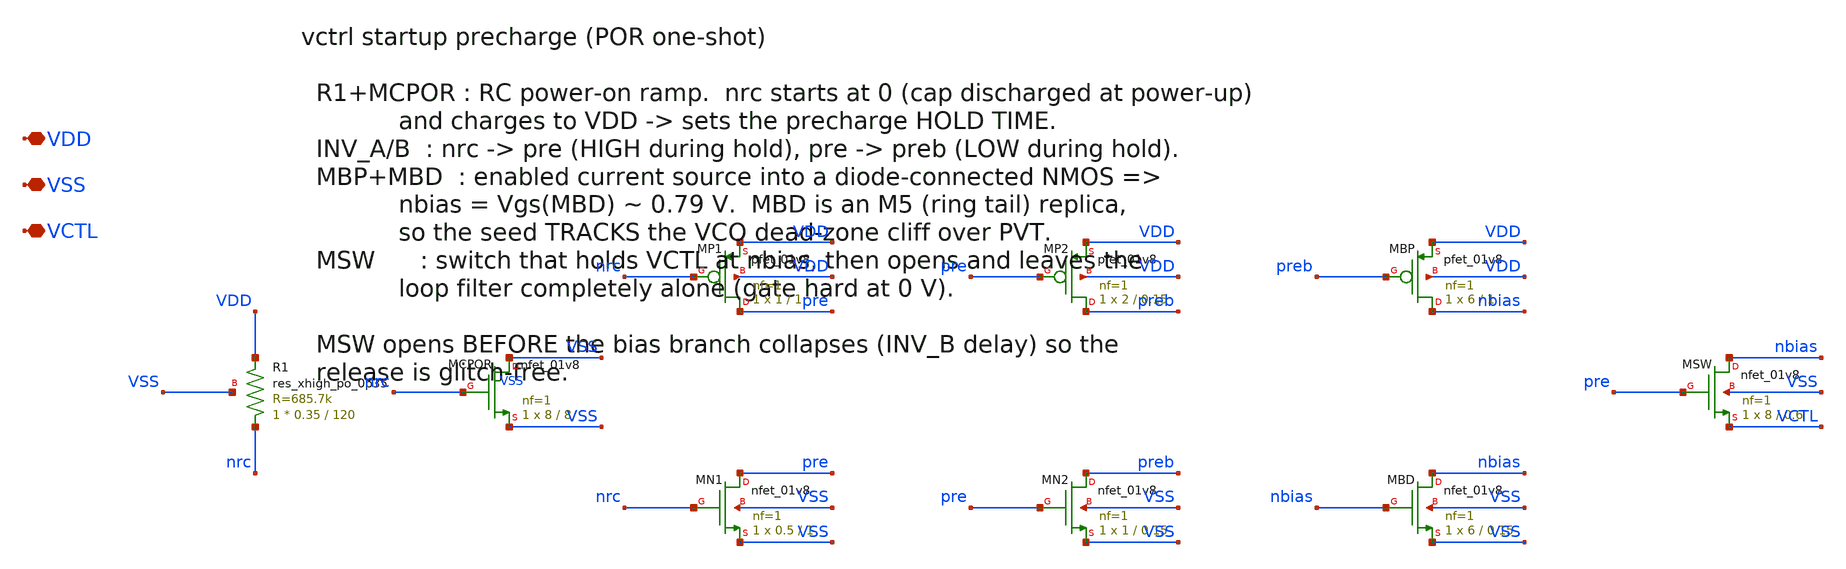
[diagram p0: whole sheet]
** sch_path: xschem/vctrl_precharge.sch
**.subckt vctrl_precharge VDD VSS VCTL
*.iopin VDD
*.iopin VSS
*.iopin VCTL
XR1 nrc VDD VSS sky130_fd_pr__res_xhigh_po_0p35 L=120 mult=1 m=1
XMCPOR VSS nrc VSS VSS sky130_fd_pr__nfet_01v8 L=8 W=8 nf=1 ad='int((nf+1)/2) * W/nf * 0.29' as='int((nf+2)/2) * W/nf * 0.29'
+ pd='2*int((nf+1)/2) * (W/nf + 0.29)' ps='2*int((nf+2)/2) * (W/nf + 0.29)' nrd='0.29 / W' nrs='0.29 / W'
+ sa=0 sb=0 sd=0 mult=1 m=1
XMP1 pre nrc VDD VDD sky130_fd_pr__pfet_01v8 L=1 W=1 nf=1 ad='int((nf+1)/2) * W/nf * 0.29' as='int((nf+2)/2) * W/nf * 0.29'
+ pd='2*int((nf+1)/2) * (W/nf + 0.29)' ps='2*int((nf+2)/2) * (W/nf + 0.29)' nrd='0.29 / W' nrs='0.29 / W'
+ sa=0 sb=0 sd=0 mult=1 m=1
XMN1 pre nrc VSS VSS sky130_fd_pr__nfet_01v8 L=1 W=0.5 nf=1 ad='int((nf+1)/2) * W/nf * 0.29' as='int((nf+2)/2) * W/nf * 0.29'
+ pd='2*int((nf+1)/2) * (W/nf + 0.29)' ps='2*int((nf+2)/2) * (W/nf + 0.29)' nrd='0.29 / W' nrs='0.29 / W'
+ sa=0 sb=0 sd=0 mult=1 m=1
XMP2 preb pre VDD VDD sky130_fd_pr__pfet_01v8 L=0.15 W=2 nf=1 ad='int((nf+1)/2) * W/nf * 0.29' as='int((nf+2)/2) * W/nf * 0.29'
+ pd='2*int((nf+1)/2) * (W/nf + 0.29)' ps='2*int((nf+2)/2) * (W/nf + 0.29)' nrd='0.29 / W' nrs='0.29 / W'
+ sa=0 sb=0 sd=0 mult=1 m=1
XMN2 preb pre VSS VSS sky130_fd_pr__nfet_01v8 L=0.15 W=1 nf=1 ad='int((nf+1)/2) * W/nf * 0.29' as='int((nf+2)/2) * W/nf * 0.29'
+ pd='2*int((nf+1)/2) * (W/nf + 0.29)' ps='2*int((nf+2)/2) * (W/nf + 0.29)' nrd='0.29 / W' nrs='0.29 / W'
+ sa=0 sb=0 sd=0 mult=1 m=1
XMBP nbias preb VDD VDD sky130_fd_pr__pfet_01v8 L=1 W=6 nf=1 ad='int((nf+1)/2) * W/nf * 0.29' as='int((nf+2)/2) * W/nf * 0.29'
+ pd='2*int((nf+1)/2) * (W/nf + 0.29)' ps='2*int((nf+2)/2) * (W/nf + 0.29)' nrd='0.29 / W' nrs='0.29 / W'
+ sa=0 sb=0 sd=0 mult=1 m=1
XMBD nbias nbias VSS VSS sky130_fd_pr__nfet_01v8 L=0.15 W=6 nf=1 ad='int((nf+1)/2) * W/nf * 0.29' as='int((nf+2)/2) * W/nf * 0.29'
+ pd='2*int((nf+1)/2) * (W/nf + 0.29)' ps='2*int((nf+2)/2) * (W/nf + 0.29)' nrd='0.29 / W' nrs='0.29 / W'
+ sa=0 sb=0 sd=0 mult=1 m=1
XMSW nbias pre VCTL VSS sky130_fd_pr__nfet_01v8 L=0.6 W=8 nf=1 ad='int((nf+1)/2) * W/nf * 0.29' as='int((nf+2)/2) * W/nf * 0.29'
+ pd='2*int((nf+1)/2) * (W/nf + 0.29)' ps='2*int((nf+2)/2) * (W/nf + 0.29)' nrd='0.29 / W' nrs='0.29 / W'
+ sa=0 sb=0 sd=0 mult=1 m=1
**.ends
.end
